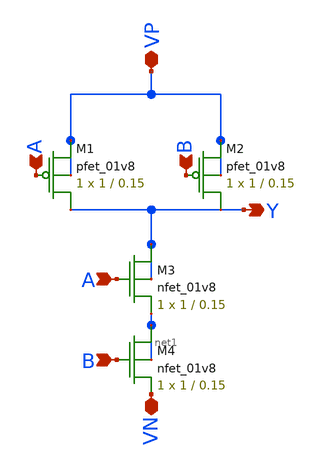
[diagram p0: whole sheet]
** sch_path: mp1/cmos_inverter/nand.sch
**.subckt nand A B Y VP VN A B
*.ipin A
*.ipin B
*.opin Y
*.iopin VP
*.iopin VN
*.ipin A
*.ipin B
XM1 Y A VP VP sky130_fd_pr__pfet_01v8 L=0.15 W=1 nf=1 ad='int((nf+1)/2) * W/nf * 0.29' as='int((nf+2)/2) * W/nf * 0.29'
+ pd='2*int((nf+1)/2) * (W/nf + 0.29)' ps='2*int((nf+2)/2) * (W/nf + 0.29)' nrd='0.29 / W' nrs='0.29 / W'
+ sa=0 sb=0 sd=0 mult=1 m=1
XM2 Y B VP VP sky130_fd_pr__pfet_01v8 L=0.15 W=1 nf=1 ad='int((nf+1)/2) * W/nf * 0.29' as='int((nf+2)/2) * W/nf * 0.29'
+ pd='2*int((nf+1)/2) * (W/nf + 0.29)' ps='2*int((nf+2)/2) * (W/nf + 0.29)' nrd='0.29 / W' nrs='0.29 / W'
+ sa=0 sb=0 sd=0 mult=1 m=1
XM3 Y A net1 Y sky130_fd_pr__nfet_01v8 L=0.15 W=1 nf=1 ad='int((nf+1)/2) * W/nf * 0.29' as='int((nf+2)/2) * W/nf * 0.29'
+ pd='2*int((nf+1)/2) * (W/nf + 0.29)' ps='2*int((nf+2)/2) * (W/nf + 0.29)' nrd='0.29 / W' nrs='0.29 / W'
+ sa=0 sb=0 sd=0 mult=1 m=1
XM4 net1 B VN net1 sky130_fd_pr__nfet_01v8 L=0.15 W=1 nf=1 ad='int((nf+1)/2) * W/nf * 0.29' as='int((nf+2)/2) * W/nf * 0.29'
+ pd='2*int((nf+1)/2) * (W/nf + 0.29)' ps='2*int((nf+2)/2) * (W/nf + 0.29)' nrd='0.29 / W' nrs='0.29 / W'
+ sa=0 sb=0 sd=0 mult=1 m=1
**.ends
.end
